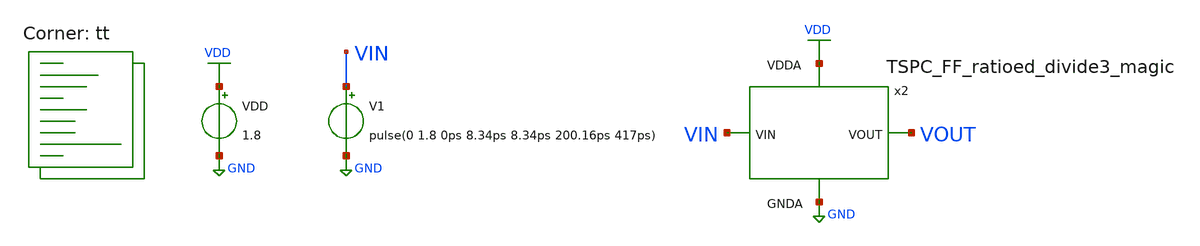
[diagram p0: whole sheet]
** sch_path: projects/pll/divider/magic/divide_by_120/tb_TSPC_FF_ratioed_divide3_magic.sch
**.subckt tb_TSPC_FF_ratioed_divide3_magic
VDD VDD GND 1.8
V1 VIN GND pulse(0 1.8 0ps 8.34ps 8.34ps 200.16ps 417ps)
x2 VOUT VIN VDD GND TSPC_FF_ratioed_divide3_magic
**** begin user architecture code




.option method=gear
.option wnflag=1


.control

  save v(vin) v(vout) p(x1:power)
  * save all
  tran 0.02p 10n

  remzerovec
  write tb_TSPC_FF_ratioed_divide3_6.raw
  set appendwrite

.endc



.lib $::SKYWATER_MODELS/sky130.lib.spice tt
**** end user architecture code
**.ends
.GLOBAL GND
.GLOBAL VDD
.end
